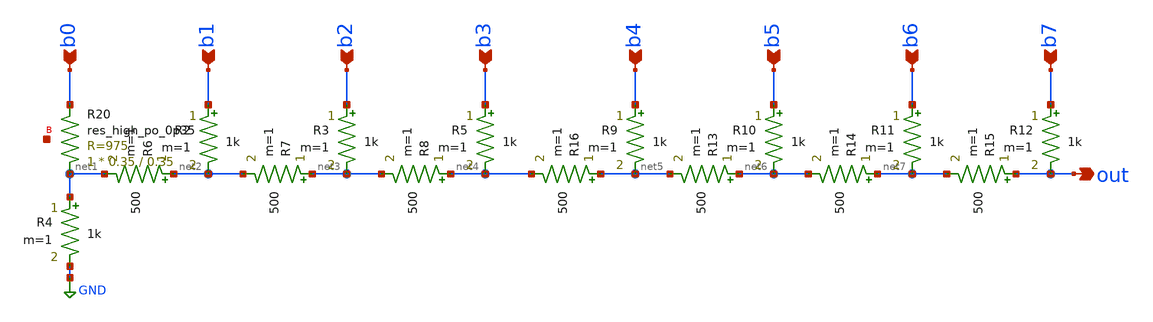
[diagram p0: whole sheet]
** sch_path: xschem/r2r.sch
**.subckt r2r b1 b0 b2 b3 b5 out b4 b6 b7
*.ipin b1
*.ipin b0
*.ipin b2
*.ipin b3
*.ipin b5
*.opin out
*.ipin b4
*.ipin b6
*.ipin b7
R2 b1 net2 1k m=1
R3 b2 net3 1k m=1
R4 net1 GND 1k m=1
R5 b3 net4 1k m=1
R6 net2 net1 500 m=1
R7 net3 net2 500 m=1
R8 net4 net3 500 m=1
R9 b4 net5 1k m=1
R10 b5 net6 1k m=1
R11 b6 net7 1k m=1
R12 b7 out 1k m=1
R13 net6 net5 500 m=1
R14 net7 net6 500 m=1
R15 out net7 500 m=1
R16 net5 net4 500 m=1
XR20 net1 b0 net8 sky130_fd_pr__res_high_po_0p35 L=0.35 mult=1 m=1
**.ends
.GLOBAL GND
.end
